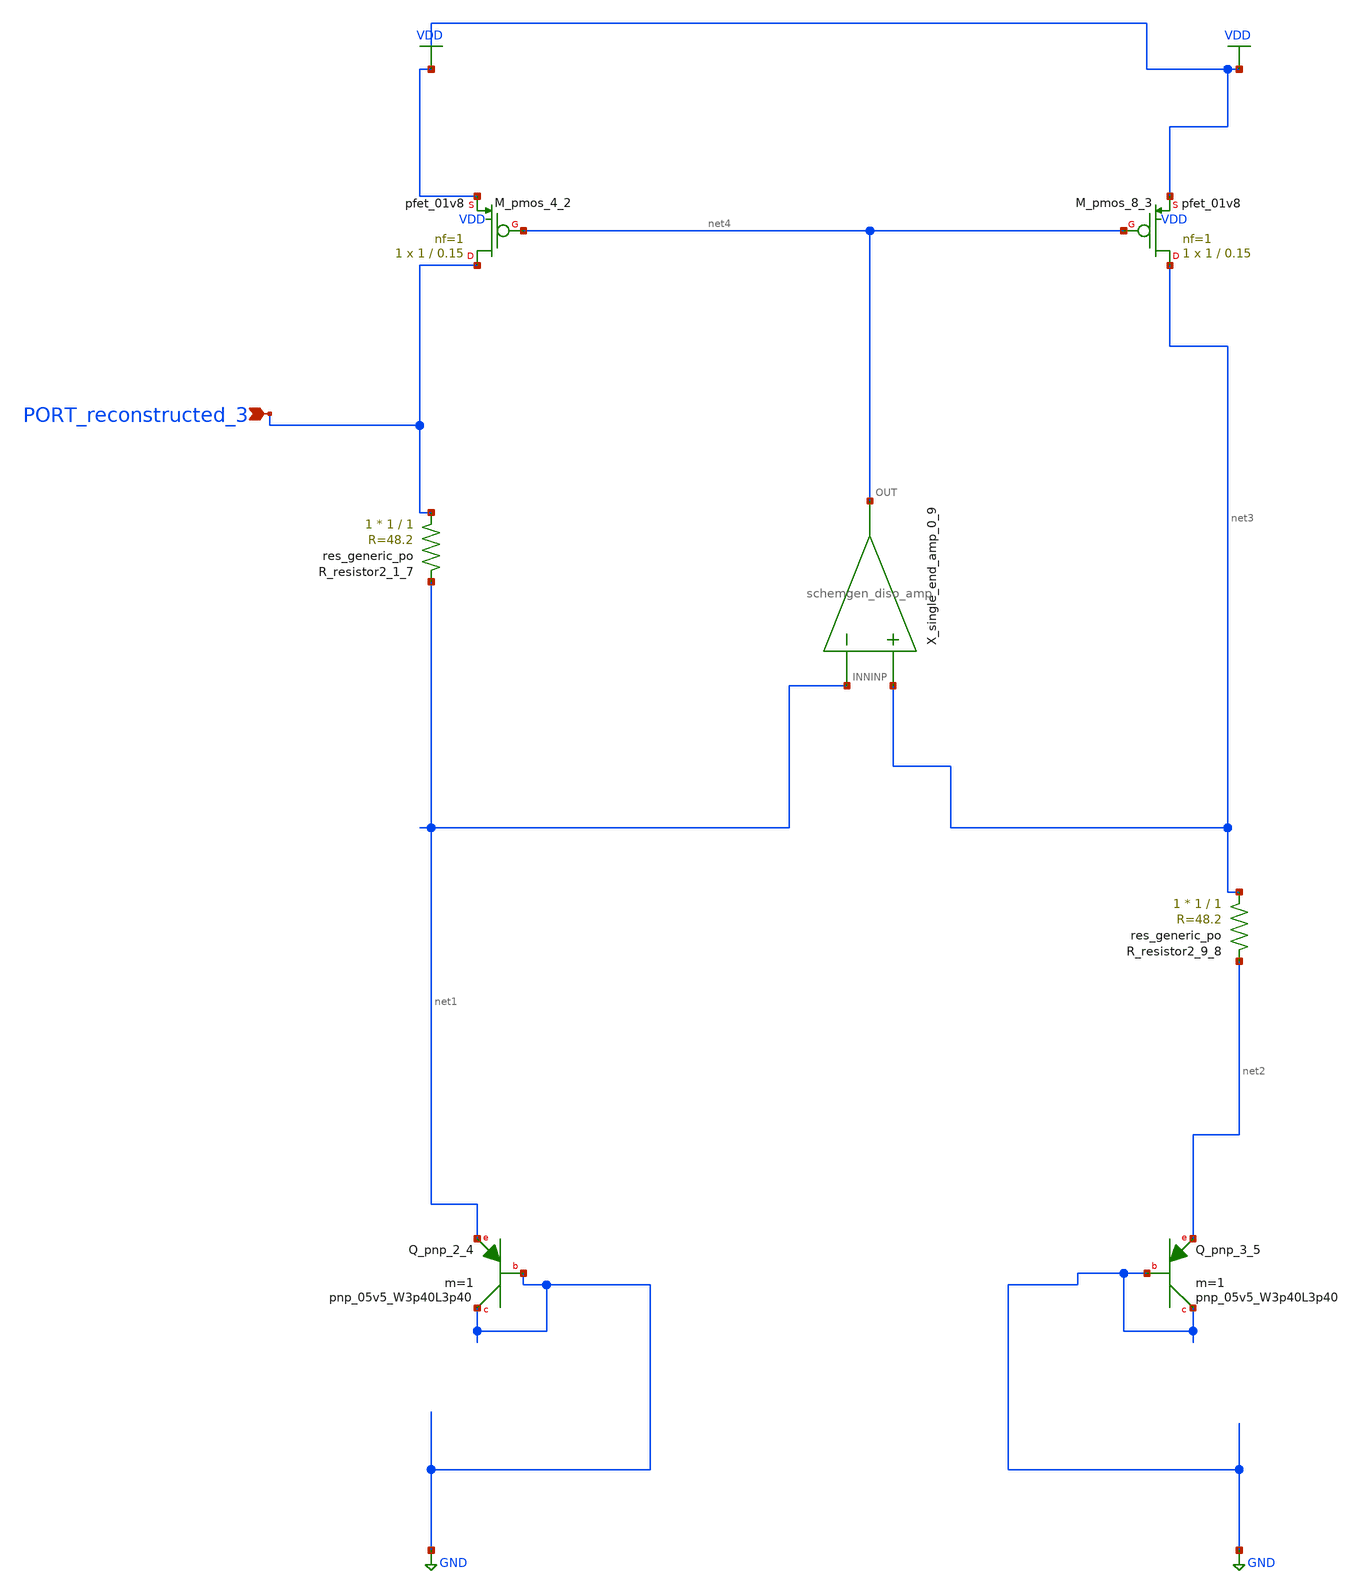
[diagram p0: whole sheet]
** sch_path: schematics/Image2Net/100.sch
**.subckt 100 PORT_reconstructed_3
*.ipin PORT_reconstructed_3
XM_pmos_4_2 PORT_reconstructed_3 net4 VDD VDD sky130_fd_pr__pfet_01v8 L=0.15 W=1 nf=1 ad='int((1 + 1)/2) * 1 / 1 * 0.29'
+ as='int((1 + 2)/2) * 1 / 1 * 0.29' pd='2*int((1 + 1)/2) * (1 / 1 + 0.29)' ps='2*int((1 + 2)/2) * (1 / 1 + 0.29)'
+ nrd='0.29 / 1 ' nrs='0.29 / 1 ' sa=0 sb=0 sd=0 mult=1 m=1
XM_pmos_8_3 net3 net4 VDD VDD sky130_fd_pr__pfet_01v8 L=0.15 W=1 nf=1 ad='int((1 + 1)/2) * 1 / 1 * 0.29'
+ as='int((1 + 2)/2) * 1 / 1 * 0.29' pd='2*int((1 + 1)/2) * (1 / 1 + 0.29)' ps='2*int((1 + 2)/2) * (1 / 1 + 0.29)'
+ nrd='0.29 / 1 ' nrs='0.29 / 1 ' sa=0 sb=0 sd=0 mult=1 m=1
XQ_pnp_2_4 GND GND net1 sky130_fd_pr__pnp_05v5_W3p40L3p40 m=1
XQ_pnp_3_5 GND GND net2 sky130_fd_pr__pnp_05v5_W3p40L3p40 m=1
XR_resistor2_1_7 PORT_reconstructed_3 net1 sky130_fd_pr__res_generic_po W=1 L=1 m=1
XR_resistor2_9_8 net3 net2 sky130_fd_pr__res_generic_po W=1 L=1 m=1
X_single_end_amp_0_9 net3 net1 net4 schemgen_diso_amp
**.ends

* expanding   symbol:  schemgen_diso_amp.sym # of pins=3
** sym_path: symbols/schemgen_diso_amp.sym
.subckt schemgen_diso_amp INP INN OUT
* SchemGen ideal op-amp: Vout = 1e5 * (V(INP) - V(INN))
E1 OUT 0 INP INN 1e5
.ends schemgen_diso_amp
.GLOBAL GND
.GLOBAL VDD
.end
